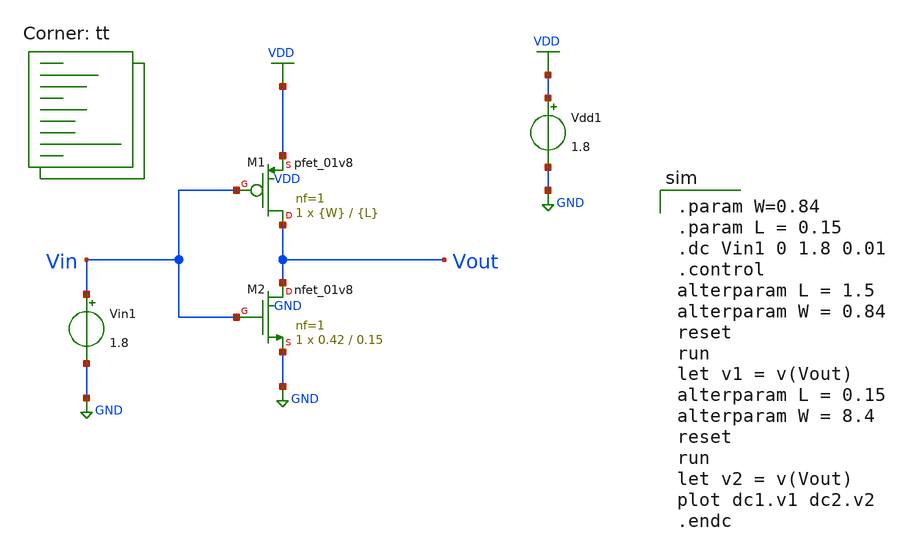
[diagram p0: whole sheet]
** sch_path: tutorial-2/source/q1b.sch
**.subckt q1b
XM1 Vout Vin VDD VDD sky130_fd_pr__pfet_01v8 L={L} W={W} nf=1 ad='int((nf+1)/2) * W/nf * 0.29' as='int((nf+2)/2) * W/nf * 0.29'
+ pd='2*int((nf+1)/2) * (W/nf + 0.29)' ps='2*int((nf+2)/2) * (W/nf + 0.29)' nrd='0.29 / W' nrs='0.29 / W'
+ sa=0 sb=0 sd=0 mult=1 m=1
XM2 Vout Vin GND GND sky130_fd_pr__nfet_01v8 L=0.15 W=0.42 nf=1 ad='int((nf+1)/2) * W/nf * 0.29' as='int((nf+2)/2) * W/nf * 0.29'
+ pd='2*int((nf+1)/2) * (W/nf + 0.29)' ps='2*int((nf+2)/2) * (W/nf + 0.29)' nrd='0.29 / W' nrs='0.29 / W'
+ sa=0 sb=0 sd=0 mult=1 m=1
Vdd1 VDD GND 1.8
Vin1 Vin GND 1.8
**** begin user architecture code
.lib $::SKYWATER_MODELS/sky130.lib.spice tt

.param W=0.84
.param L = 0.15
.dc Vin1 0 1.8 0.01
.control
alterparam L = 1.5
alterparam W = 0.84
reset
run
let v1 = v(Vout)
alterparam L = 0.15
alterparam W = 8.4
reset
run
let v2 = v(Vout)
plot dc1.v1 dc2.v2
.endc

**** end user architecture code
**.ends
.GLOBAL VDD
.GLOBAL GND
.end
